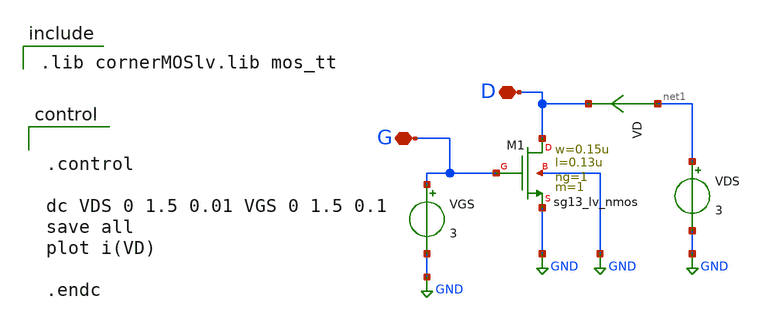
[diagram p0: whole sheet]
** sch_path: designs/nmos/nmos.sch
**.subckt nmos D G
*.iopin D
*.iopin G
XM1 D G GND GND sg13_lv_nmos w=0.15u l=0.13u ng=1 m=1 mm_ok=1
VGS G GND 3
VDS net1 GND 3
VD net1 D 0
.save i(vd)
**** begin user architecture code

.lib cornerMOSlv.lib mos_tt



.control

dc VDS 0 1.5 0.01 VGS 0 1.5 0.1
save all
plot i(VD)

.endc


**** end user architecture code
**.ends
.GLOBAL GND
.end
